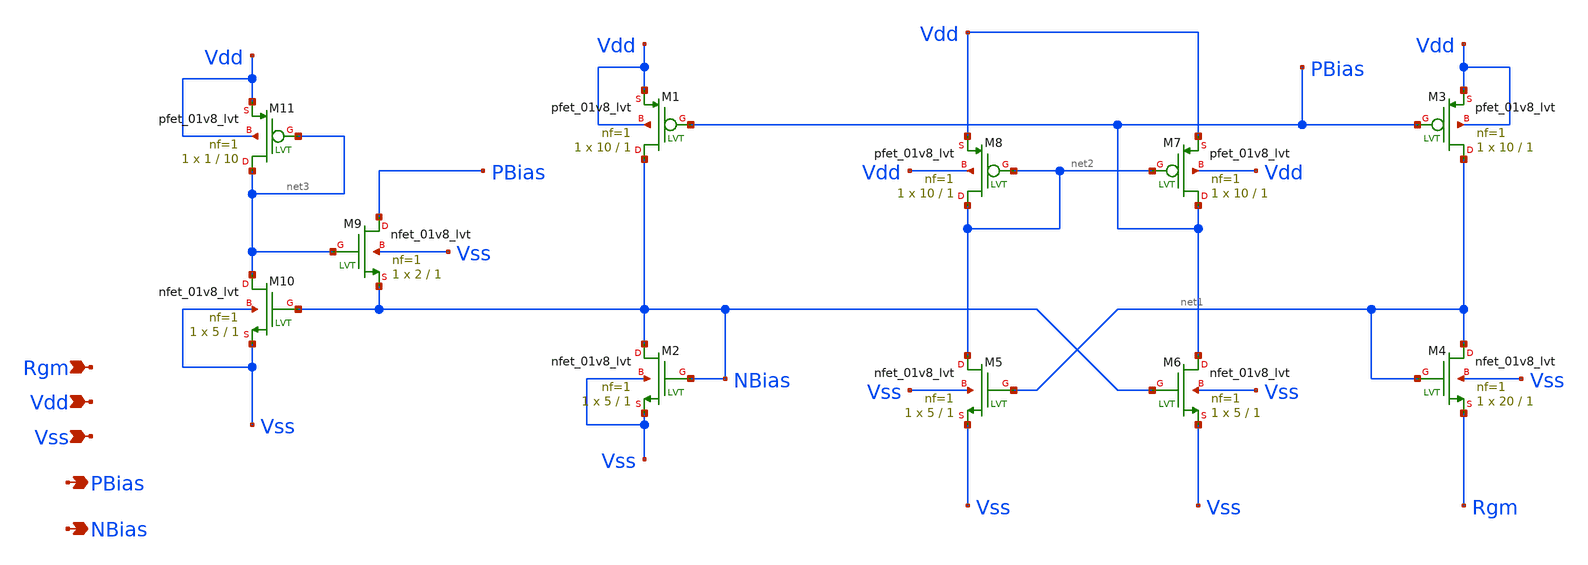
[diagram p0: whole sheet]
** sch_path: src/Opamp_Design/src/Beta_Multiplier.sch
**.subckt Beta_Multiplier Vdd PBias Vss NBias Rgm
*.ipin Vdd
*.opin PBias
*.ipin Vss
*.opin NBias
*.ipin Rgm
XM1 NBias PBias Vdd Vdd sky130_fd_pr__pfet_01v8_lvt L=1 W=10 nf=1 ad='int((nf+1)/2) * W/nf * 0.29' as='int((nf+2)/2) * W/nf * 0.29'
+ pd='2*int((nf+1)/2) * (W/nf + 0.29)' ps='2*int((nf+2)/2) * (W/nf + 0.29)' nrd='0.29 / W' nrs='0.29 / W'
+ sa=0 sb=0 sd=0 mult=1 m=1
XM2 NBias NBias Vss Vss sky130_fd_pr__nfet_01v8_lvt L=1 W=5 nf=1 ad='int((nf+1)/2) * W/nf * 0.29' as='int((nf+2)/2) * W/nf * 0.29'
+ pd='2*int((nf+1)/2) * (W/nf + 0.29)' ps='2*int((nf+2)/2) * (W/nf + 0.29)' nrd='0.29 / W' nrs='0.29 / W'
+ sa=0 sb=0 sd=0 mult=1 m=1
XM3 net1 PBias Vdd Vdd sky130_fd_pr__pfet_01v8_lvt L=1 W=10 nf=1 ad='int((nf+1)/2) * W/nf * 0.29' as='int((nf+2)/2) * W/nf * 0.29'
+ pd='2*int((nf+1)/2) * (W/nf + 0.29)' ps='2*int((nf+2)/2) * (W/nf + 0.29)' nrd='0.29 / W' nrs='0.29 / W'
+ sa=0 sb=0 sd=0 mult=1 m=1
XM4 net1 net1 Rgm Vss sky130_fd_pr__nfet_01v8_lvt L=1 W=20 nf=1 ad='int((nf+1)/2) * W/nf * 0.29' as='int((nf+2)/2) * W/nf * 0.29'
+ pd='2*int((nf+1)/2) * (W/nf + 0.29)' ps='2*int((nf+2)/2) * (W/nf + 0.29)' nrd='0.29 / W' nrs='0.29 / W'
+ sa=0 sb=0 sd=0 mult=1 m=1
XM5 net2 net1 Vss Vss sky130_fd_pr__nfet_01v8_lvt L=1 W=5 nf=1 ad='int((nf+1)/2) * W/nf * 0.29' as='int((nf+2)/2) * W/nf * 0.29'
+ pd='2*int((nf+1)/2) * (W/nf + 0.29)' ps='2*int((nf+2)/2) * (W/nf + 0.29)' nrd='0.29 / W' nrs='0.29 / W'
+ sa=0 sb=0 sd=0 mult=1 m=1
XM6 PBias NBias Vss Vss sky130_fd_pr__nfet_01v8_lvt L=1 W=5 nf=1 ad='int((nf+1)/2) * W/nf * 0.29' as='int((nf+2)/2) * W/nf * 0.29'
+ pd='2*int((nf+1)/2) * (W/nf + 0.29)' ps='2*int((nf+2)/2) * (W/nf + 0.29)' nrd='0.29 / W' nrs='0.29 / W'
+ sa=0 sb=0 sd=0 mult=1 m=1
XM7 PBias net2 Vdd Vdd sky130_fd_pr__pfet_01v8_lvt L=1 W=10 nf=1 ad='int((nf+1)/2) * W/nf * 0.29' as='int((nf+2)/2) * W/nf * 0.29'
+ pd='2*int((nf+1)/2) * (W/nf + 0.29)' ps='2*int((nf+2)/2) * (W/nf + 0.29)' nrd='0.29 / W' nrs='0.29 / W'
+ sa=0 sb=0 sd=0 mult=1 m=1
XM8 net2 net2 Vdd Vdd sky130_fd_pr__pfet_01v8_lvt L=1 W=10 nf=1 ad='int((nf+1)/2) * W/nf * 0.29' as='int((nf+2)/2) * W/nf * 0.29'
+ pd='2*int((nf+1)/2) * (W/nf + 0.29)' ps='2*int((nf+2)/2) * (W/nf + 0.29)' nrd='0.29 / W' nrs='0.29 / W'
+ sa=0 sb=0 sd=0 mult=1 m=1
XM9 PBias net3 NBias Vss sky130_fd_pr__nfet_01v8_lvt L=1 W=2 nf=1 ad='int((nf+1)/2) * W/nf * 0.29' as='int((nf+2)/2) * W/nf * 0.29'
+ pd='2*int((nf+1)/2) * (W/nf + 0.29)' ps='2*int((nf+2)/2) * (W/nf + 0.29)' nrd='0.29 / W' nrs='0.29 / W'
+ sa=0 sb=0 sd=0 mult=1 m=1
XM10 net3 NBias Vss Vss sky130_fd_pr__nfet_01v8_lvt L=1 W=5 nf=1 ad='int((nf+1)/2) * W/nf * 0.29' as='int((nf+2)/2) * W/nf * 0.29'
+ pd='2*int((nf+1)/2) * (W/nf + 0.29)' ps='2*int((nf+2)/2) * (W/nf + 0.29)' nrd='0.29 / W' nrs='0.29 / W'
+ sa=0 sb=0 sd=0 mult=1 m=1
XM11 net3 net3 Vdd Vdd sky130_fd_pr__pfet_01v8_lvt L=10 W=1 nf=1 ad='int((nf+1)/2) * W/nf * 0.29' as='int((nf+2)/2) * W/nf * 0.29'
+ pd='2*int((nf+1)/2) * (W/nf + 0.29)' ps='2*int((nf+2)/2) * (W/nf + 0.29)' nrd='0.29 / W' nrs='0.29 / W'
+ sa=0 sb=0 sd=0 mult=1 m=1
**.ends
.end
